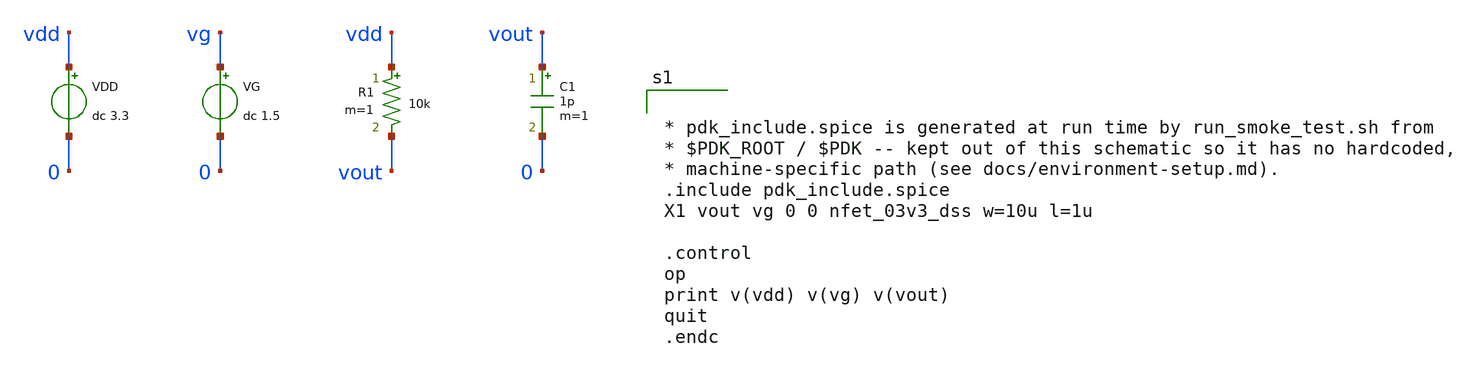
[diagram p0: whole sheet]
** sch_path: design/smoke_test.sch
**.subckt smoke_test
VDD vdd 0 dc 3.3
VG vg 0 dc 1.5
R1 vdd vout 10k m=1
C1 vout 0 1p m=1
**** begin user architecture code


* pdk_include.spice is generated at run time by run_smoke_test.sh from
* $PDK_ROOT / $PDK -- kept out of this schematic so it has no hardcoded,
* machine-specific path (see docs/environment-setup.md).
.include pdk_include.spice
X1 vout vg 0 0 nfet_03v3_dss w=10u l=1u

.control
op
print v(vdd) v(vg) v(vout)
quit
.endc


**** end user architecture code
**.ends
.end
